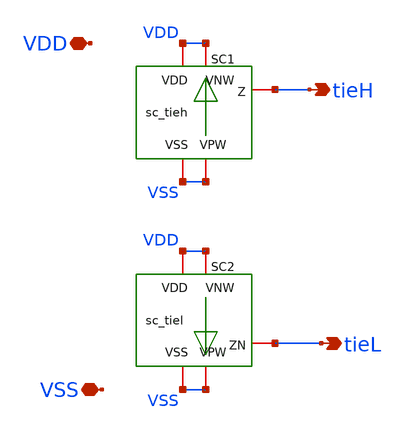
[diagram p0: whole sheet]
** sch_path: designs/libs/A1_core/top_tieh_tiel/sc_tieh_tiel.sch
**.subckt sc_tieh_tiel VDD VSS tieH tieL
*.iopin VDD
*.iopin VSS
*.opin tieH
*.opin tieL
XSC1 tieH VDD VDD VSS VSS gf180mcu_fd_sc_mcu9t5v0__tieh
XSC2 tieL VDD VDD VSS VSS gf180mcu_fd_sc_mcu9t5v0__tiel
**.ends
.end
